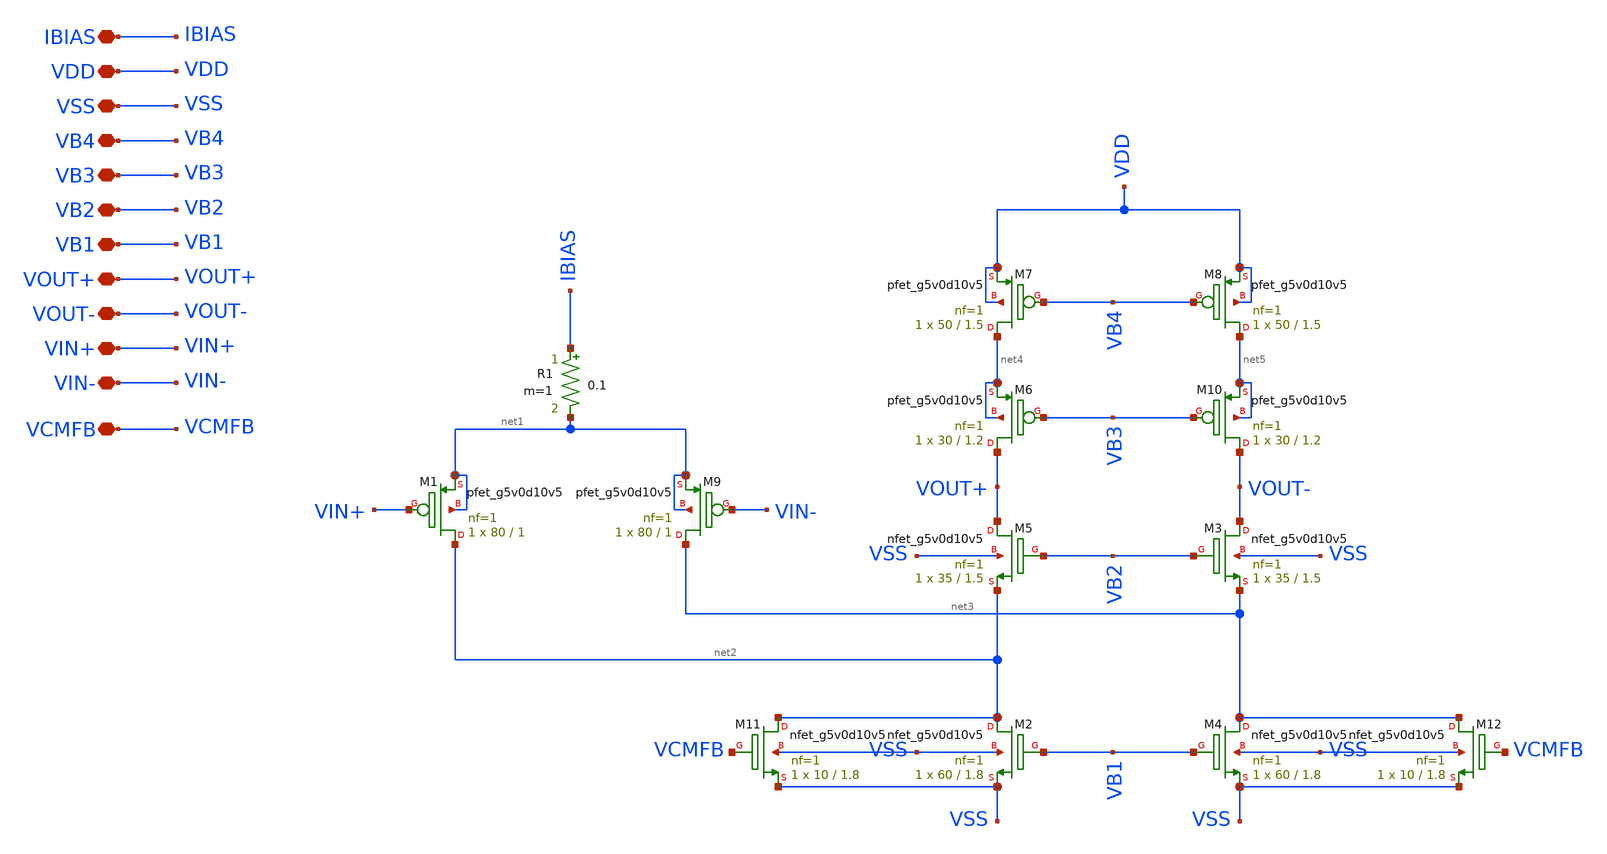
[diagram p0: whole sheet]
** sch_path: folded_cascode_amplifier_upgraded/1_stage/1stage.sch
**.subckt 1stage IBIAS VDD VB4 VB3 VB2 VB1 VSS VOUT+ VOUT- VIN+ VIN- VCMFB
*.iopin IBIAS
*.iopin VDD
*.iopin VB4
*.iopin VB3
*.iopin VB2
*.iopin VB1
*.iopin VSS
*.iopin VOUT+
*.iopin VOUT-
*.iopin VIN+
*.iopin VIN-
*.iopin VCMFB
XM9 net3 VIN- net1 net1 sky130_fd_pr__pfet_g5v0d10v5 L=1 W=80 nf=1 ad='int((1 + 1)/2) * 80 / 1 * 0.29'
+ as='int((1 + 2)/2) * 80 / 1 * 0.29' pd='2*int((1 + 1)/2) * (80 / 1 + 0.29)' ps='2*int((1 + 2)/2) * (80 / 1 + 0.29)'
+ nrd='0.29 / 80 ' nrs='0.29 / 80 ' sa=0 sb=0 sd=0 mult=1 m=1
XM1 net2 VIN+ net1 net1 sky130_fd_pr__pfet_g5v0d10v5 L=1 W=80 nf=1 ad='int((1 + 1)/2) * 80 / 1 * 0.29'
+ as='int((1 + 2)/2) * 80 / 1 * 0.29' pd='2*int((1 + 1)/2) * (80 / 1 + 0.29)' ps='2*int((1 + 2)/2) * (80 / 1 + 0.29)'
+ nrd='0.29 / 80 ' nrs='0.29 / 80 ' sa=0 sb=0 sd=0 mult=1 m=1
R1 IBIAS net1 0.1 m=1
XM5 VOUT+ VB2 net2 VSS sky130_fd_pr__nfet_g5v0d10v5 L=1.5 W=35 nf=1 ad='int((1 + 1)/2) * 35 / 1 * 0.29'
+ as='int((1 + 2)/2) * 35 / 1 * 0.29' pd='2*int((1 + 1)/2) * (35 / 1 + 0.29)' ps='2*int((1 + 2)/2) * (35 / 1 + 0.29)'
+ nrd='0.29 / 35 ' nrs='0.29 / 35 ' sa=0 sb=0 sd=0 mult=1 m=1
XM2 net2 VB1 VSS VSS sky130_fd_pr__nfet_g5v0d10v5 L=1.8 W=60 nf=1 ad='int((1 + 1)/2) * 60 / 1 * 0.29'
+ as='int((1 + 2)/2) * 60 / 1 * 0.29' pd='2*int((1 + 1)/2) * (60 / 1 + 0.29)' ps='2*int((1 + 2)/2) * (60 / 1 + 0.29)'
+ nrd='0.29 / 60 ' nrs='0.29 / 60 ' sa=0 sb=0 sd=0 mult=1 m=1
XM3 VOUT- VB2 net3 VSS sky130_fd_pr__nfet_g5v0d10v5 L=1.5 W=35 nf=1 ad='int((1 + 1)/2) * 35 / 1 * 0.29'
+ as='int((1 + 2)/2) * 35 / 1 * 0.29' pd='2*int((1 + 1)/2) * (35 / 1 + 0.29)' ps='2*int((1 + 2)/2) * (35 / 1 + 0.29)'
+ nrd='0.29 / 35 ' nrs='0.29 / 35 ' sa=0 sb=0 sd=0 mult=1 m=1
XM4 net3 VB1 VSS VSS sky130_fd_pr__nfet_g5v0d10v5 L=1.8 W=60 nf=1 ad='int((1 + 1)/2) * 60 / 1 * 0.29'
+ as='int((1 + 2)/2) * 60 / 1 * 0.29' pd='2*int((1 + 1)/2) * (60 / 1 + 0.29)' ps='2*int((1 + 2)/2) * (60 / 1 + 0.29)'
+ nrd='0.29 / 60 ' nrs='0.29 / 60 ' sa=0 sb=0 sd=0 mult=1 m=1
XM6 VOUT+ VB3 net4 net4 sky130_fd_pr__pfet_g5v0d10v5 L=1.2 W=30 nf=1 ad='int((1 + 1)/2) * 30 / 1 * 0.29'
+ as='int((1 + 2)/2) * 30 / 1 * 0.29' pd='2*int((1 + 1)/2) * (30 / 1 + 0.29)' ps='2*int((1 + 2)/2) * (30 / 1 + 0.29)'
+ nrd='0.29 / 30 ' nrs='0.29 / 30 ' sa=0 sb=0 sd=0 mult=1 m=1
XM7 net4 VB4 VDD VDD sky130_fd_pr__pfet_g5v0d10v5 L=1.5 W=50 nf=1 ad='int((1 + 1)/2) * 50 / 1 * 0.29'
+ as='int((1 + 2)/2) * 50 / 1 * 0.29' pd='2*int((1 + 1)/2) * (50 / 1 + 0.29)' ps='2*int((1 + 2)/2) * (50 / 1 + 0.29)'
+ nrd='0.29 / 50 ' nrs='0.29 / 50 ' sa=0 sb=0 sd=0 mult=1 m=1
XM8 net5 VB4 VDD VDD sky130_fd_pr__pfet_g5v0d10v5 L=1.5 W=50 nf=1 ad='int((1 + 1)/2) * 50 / 1 * 0.29'
+ as='int((1 + 2)/2) * 50 / 1 * 0.29' pd='2*int((1 + 1)/2) * (50 / 1 + 0.29)' ps='2*int((1 + 2)/2) * (50 / 1 + 0.29)'
+ nrd='0.29 / 50 ' nrs='0.29 / 50 ' sa=0 sb=0 sd=0 mult=1 m=1
XM10 VOUT- VB3 net5 net5 sky130_fd_pr__pfet_g5v0d10v5 L=1.2 W=30 nf=1 ad='int((1 + 1)/2) * 30 / 1 * 0.29'
+ as='int((1 + 2)/2) * 30 / 1 * 0.29' pd='2*int((1 + 1)/2) * (30 / 1 + 0.29)' ps='2*int((1 + 2)/2) * (30 / 1 + 0.29)'
+ nrd='0.29 / 30 ' nrs='0.29 / 30 ' sa=0 sb=0 sd=0 mult=1 m=1
XM11 net2 VCMFB VSS VSS sky130_fd_pr__nfet_g5v0d10v5 L=1.8 W=10 nf=1 ad='int((1 + 1)/2) * 10 / 1 * 0.29'
+ as='int((1 + 2)/2) * 10 / 1 * 0.29' pd='2*int((1 + 1)/2) * (10 / 1 + 0.29)' ps='2*int((1 + 2)/2) * (10 / 1 + 0.29)'
+ nrd='0.29 / 10 ' nrs='0.29 / 10 ' sa=0 sb=0 sd=0 mult=1 m=1
XM12 net3 VCMFB VSS VSS sky130_fd_pr__nfet_g5v0d10v5 L=1.8 W=10 nf=1 ad='int((1 + 1)/2) * 10 / 1 * 0.29'
+ as='int((1 + 2)/2) * 10 / 1 * 0.29' pd='2*int((1 + 1)/2) * (10 / 1 + 0.29)' ps='2*int((1 + 2)/2) * (10 / 1 + 0.29)'
+ nrd='0.29 / 10 ' nrs='0.29 / 10 ' sa=0 sb=0 sd=0 mult=1 m=1
**.ends
.end
